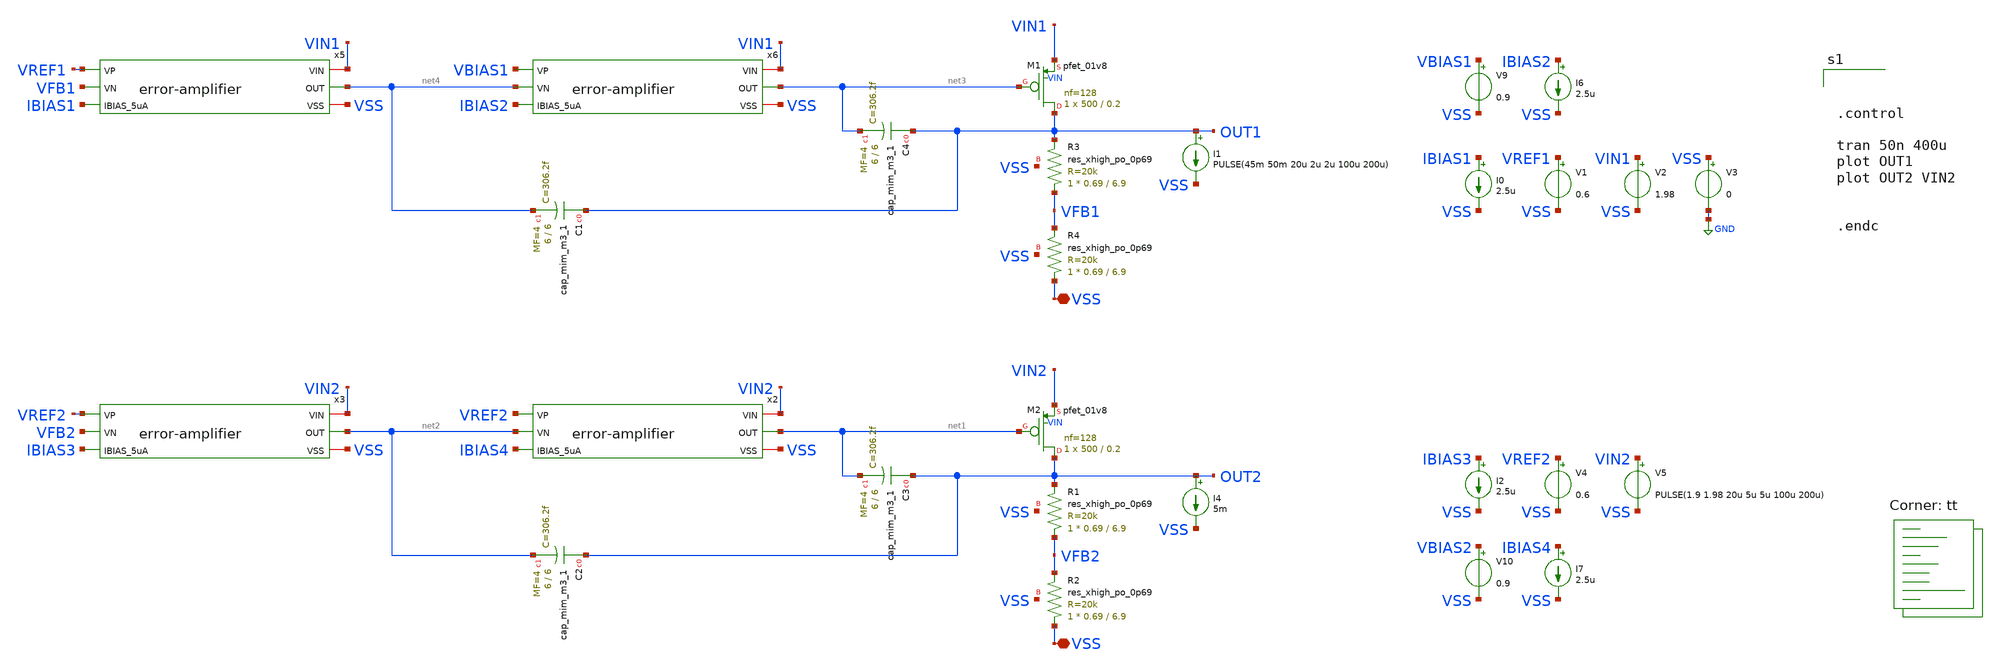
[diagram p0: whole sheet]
** sch_path: xschem/ldo_andriansyah/testbench/line-load-transient.sch
**.subckt line-load-transient VSS VSS
*.iopin VSS
*.iopin VSS
I0 IBIAS1 VSS 2.5u
V1 VREF1 VSS 0.6
V2 VIN1 VSS 1.98
V3 VSS GND 0
I1 OUT1 VSS PULSE(45m 50m 20u 2u 2u 100u 200u)
I2 IBIAS3 VSS 2.5u
V4 VREF2 VSS 0.6
V5 VIN2 VSS PULSE(1.9 1.98 20u 5u 5u 100u 200u)
V9 VBIAS1 VSS 0.9
V10 VBIAS2 VSS 0.9
I6 IBIAS2 VSS 2.5u
I7 IBIAS4 VSS 2.5u
I4 OUT2 VSS 5m
XC2 OUT2 net2 sky130_fd_pr__cap_mim_m3_1 W=6 L=6 MF=4 m=4
XC3 OUT2 net1 sky130_fd_pr__cap_mim_m3_1 W=6 L=6 MF=4 m=4
x3 VIN2 VREF2 VFB2 IBIAS3 net2 VSS error-amplifier
XR1 VFB2 OUT2 VSS sky130_fd_pr__res_xhigh_po_0p69 L=6.9 mult=1 m=1
XR2 VSS VFB2 VSS sky130_fd_pr__res_xhigh_po_0p69 L=6.9 mult=1 m=1
XM2 OUT2 net1 VIN2 VIN sky130_fd_pr__pfet_01v8 L=0.2 W=500 nf=128 ad='int((nf+1)/2) * W/nf * 0.29' as='int((nf+2)/2) * W/nf * 0.29'
+ pd='2*int((nf+1)/2) * (W/nf + 0.29)' ps='2*int((nf+2)/2) * (W/nf + 0.29)' nrd='0.29 / W' nrs='0.29 / W'
+ sa=0 sb=0 sd=0 mult=1 m=1
x2 VIN2 VREF2 net2 IBIAS4 net1 VSS error-amplifier
XC1 OUT1 net4 sky130_fd_pr__cap_mim_m3_1 W=6 L=6 MF=4 m=4
XC4 OUT1 net3 sky130_fd_pr__cap_mim_m3_1 W=6 L=6 MF=4 m=4
x5 VIN1 VREF1 VFB1 IBIAS1 net4 VSS error-amplifier
XR3 VFB1 OUT1 VSS sky130_fd_pr__res_xhigh_po_0p69 L=6.9 mult=1 m=1
XR4 VSS VFB1 VSS sky130_fd_pr__res_xhigh_po_0p69 L=6.9 mult=1 m=1
XM1 OUT1 net3 VIN1 VIN sky130_fd_pr__pfet_01v8 L=0.2 W=500 nf=128 ad='int((nf+1)/2) * W/nf * 0.29' as='int((nf+2)/2) * W/nf * 0.29'
+ pd='2*int((nf+1)/2) * (W/nf + 0.29)' ps='2*int((nf+2)/2) * (W/nf + 0.29)' nrd='0.29 / W' nrs='0.29 / W'
+ sa=0 sb=0 sd=0 mult=1 m=1
x6 VIN1 VBIAS1 net4 IBIAS2 net3 VSS error-amplifier
**** begin user architecture code



.control

tran 50n 400u
plot OUT1
plot OUT2 VIN2


.endc




.lib $::SKYWATER_MODELS/sky130.lib.spice tt
**** end user architecture code
**.ends

* expanding   symbol:
*+  /foss/designs/2026/tt_sky26b_ldo_andriansyah/xschem/error-amplifier/error-amplifier.sym # of pins=6
** sym_path: xschem/error-amplifier/error-amplifier.sym
** sch_path: xschem/error-amplifier/error-amplifier.sch
.subckt error-amplifier VIN VP VN IBIAS_5uA OUT VSS
*.ipin IBIAS_5uA
*.ipin VN
*.ipin VP
*.iopin VIN
*.iopin VSS
*.opin OUT
XM1 net2 net2 VSS VSS sky130_fd_pr__nfet_01v8 L=0.6 W=4.2 nf=4 ad='int((nf+1)/2) * W/nf * 0.29' as='int((nf+2)/2) * W/nf * 0.29'
+ pd='2*int((nf+1)/2) * (W/nf + 0.29)' ps='2*int((nf+2)/2) * (W/nf + 0.29)' nrd='0.29 / W' nrs='0.29 / W'
+ sa=0 sb=0 sd=0 mult=1 m=1
XM2 OUT net2 VSS VSS sky130_fd_pr__nfet_01v8 L=0.6 W=4.2 nf=4 ad='int((nf+1)/2) * W/nf * 0.29' as='int((nf+2)/2) * W/nf * 0.29'
+ pd='2*int((nf+1)/2) * (W/nf + 0.29)' ps='2*int((nf+2)/2) * (W/nf + 0.29)' nrd='0.29 / W' nrs='0.29 / W'
+ sa=0 sb=0 sd=0 mult=1 m=1
XM3 net2 VN net1 VDD sky130_fd_pr__pfet_01v8 L=0.6 W=28 nf=4 ad='int((nf+1)/2) * W/nf * 0.29' as='int((nf+2)/2) * W/nf * 0.29'
+ pd='2*int((nf+1)/2) * (W/nf + 0.29)' ps='2*int((nf+2)/2) * (W/nf + 0.29)' nrd='0.29 / W' nrs='0.29 / W'
+ sa=0 sb=0 sd=0 mult=1 m=1
XM4 OUT VP net1 VDD sky130_fd_pr__pfet_01v8 L=0.6 W=28 nf=4 ad='int((nf+1)/2) * W/nf * 0.29' as='int((nf+2)/2) * W/nf * 0.29'
+ pd='2*int((nf+1)/2) * (W/nf + 0.29)' ps='2*int((nf+2)/2) * (W/nf + 0.29)' nrd='0.29 / W' nrs='0.29 / W'
+ sa=0 sb=0 sd=0 mult=1 m=1
XM5 net1 IBIAS_5uA VIN VIN sky130_fd_pr__pfet_01v8 L=0.6 W=6.6 nf=4 ad='int((nf+1)/2) * W/nf * 0.29'
+ as='int((nf+2)/2) * W/nf * 0.29' pd='2*int((nf+1)/2) * (W/nf + 0.29)' ps='2*int((nf+2)/2) * (W/nf + 0.29)'
+ nrd='0.29 / W' nrs='0.29 / W' sa=0 sb=0 sd=0 mult=1 m=1
XM6 IBIAS_5uA IBIAS_5uA VIN VIN sky130_fd_pr__pfet_01v8 L=0.6 W=6.6 nf=4 ad='int((nf+1)/2) * W/nf * 0.29'
+ as='int((nf+2)/2) * W/nf * 0.29' pd='2*int((nf+1)/2) * (W/nf + 0.29)' ps='2*int((nf+2)/2) * (W/nf + 0.29)'
+ nrd='0.29 / W' nrs='0.29 / W' sa=0 sb=0 sd=0 mult=1 m=1
XM7 VDD VDD VDD VDD sky130_fd_pr__pfet_01v8 L=0.6 W=7 nf=1 ad='int((nf+1)/2) * W/nf * 0.29' as='int((nf+2)/2) * W/nf * 0.29'
+ pd='2*int((nf+1)/2) * (W/nf + 0.29)' ps='2*int((nf+2)/2) * (W/nf + 0.29)' nrd='0.29 / W' nrs='0.29 / W'
+ sa=0 sb=0 sd=0 mult=1 m=1
XM8 VSS VSS VSS VSS sky130_fd_pr__nfet_01v8 L=0.6 W=1.05 nf=1 ad='int((nf+1)/2) * W/nf * 0.29' as='int((nf+2)/2) * W/nf * 0.29'
+ pd='2*int((nf+1)/2) * (W/nf + 0.29)' ps='2*int((nf+2)/2) * (W/nf + 0.29)' nrd='0.29 / W' nrs='0.29 / W'
+ sa=0 sb=0 sd=0 mult=1 m=1
XM9 VDD VDD VDD VDD sky130_fd_pr__pfet_01v8 L=0.6 W=1.65 nf=1 ad='int((nf+1)/2) * W/nf * 0.29' as='int((nf+2)/2) * W/nf * 0.29'
+ pd='2*int((nf+1)/2) * (W/nf + 0.29)' ps='2*int((nf+2)/2) * (W/nf + 0.29)' nrd='0.29 / W' nrs='0.29 / W'
+ sa=0 sb=0 sd=0 mult=1 m=1
XM10 VSS VSS VSS VSS sky130_fd_pr__nfet_01v8 L=0.6 W=1.05 nf=1 ad='int((nf+1)/2) * W/nf * 0.29' as='int((nf+2)/2) * W/nf * 0.29'
+ pd='2*int((nf+1)/2) * (W/nf + 0.29)' ps='2*int((nf+2)/2) * (W/nf + 0.29)' nrd='0.29 / W' nrs='0.29 / W'
+ sa=0 sb=0 sd=0 mult=1 m=1
XM11 VDD VDD VDD VDD sky130_fd_pr__pfet_01v8 L=0.6 W=7 nf=1 ad='int((nf+1)/2) * W/nf * 0.29' as='int((nf+2)/2) * W/nf * 0.29'
+ pd='2*int((nf+1)/2) * (W/nf + 0.29)' ps='2*int((nf+2)/2) * (W/nf + 0.29)' nrd='0.29 / W' nrs='0.29 / W'
+ sa=0 sb=0 sd=0 mult=1 m=1
XM12 VDD VDD VDD VDD sky130_fd_pr__pfet_01v8 L=0.6 W=1.65 nf=1 ad='int((nf+1)/2) * W/nf * 0.29' as='int((nf+2)/2) * W/nf * 0.29'
+ pd='2*int((nf+1)/2) * (W/nf + 0.29)' ps='2*int((nf+2)/2) * (W/nf + 0.29)' nrd='0.29 / W' nrs='0.29 / W'
+ sa=0 sb=0 sd=0 mult=1 m=1
.ends

.GLOBAL GND
.end
